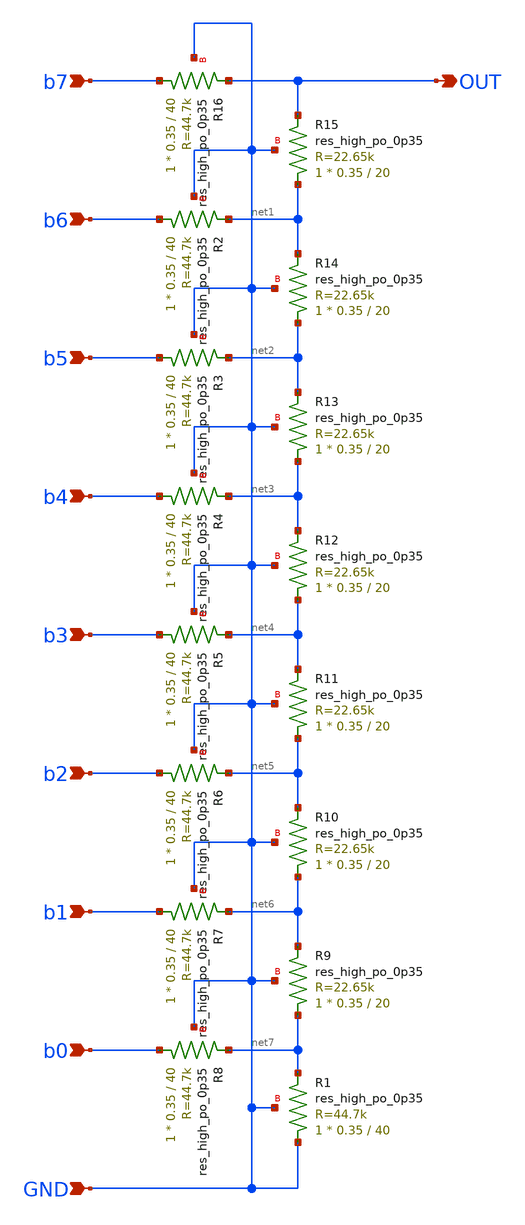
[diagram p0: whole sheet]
** sch_path: xschem/r2rdac.sch
**.subckt r2rdac b7 b6 b5 b4 b3 b2 b1 b0 GND OUT
*.ipin b7
*.ipin b6
*.ipin b5
*.ipin b4
*.ipin b3
*.ipin b2
*.ipin b1
*.ipin b0
*.ipin GND
*.opin OUT
XR16 b7 OUT GND sky130_fd_pr__res_high_po_0p35 L=40 mult=1 m=1
XR2 b6 net1 GND sky130_fd_pr__res_high_po_0p35 L=40 mult=1 m=1
XR3 b5 net2 GND sky130_fd_pr__res_high_po_0p35 L=40 mult=1 m=1
XR4 b4 net3 GND sky130_fd_pr__res_high_po_0p35 L=40 mult=1 m=1
XR5 b3 net4 GND sky130_fd_pr__res_high_po_0p35 L=40 mult=1 m=1
XR6 b2 net5 GND sky130_fd_pr__res_high_po_0p35 L=40 mult=1 m=1
XR7 b1 net6 GND sky130_fd_pr__res_high_po_0p35 L=40 mult=1 m=1
XR8 b0 net7 GND sky130_fd_pr__res_high_po_0p35 L=40 mult=1 m=1
XR1 GND net7 GND sky130_fd_pr__res_high_po_0p35 L=40 mult=1 m=1
XR9 net7 net6 GND sky130_fd_pr__res_high_po_0p35 L=20 mult=1 m=1
XR10 net6 net5 GND sky130_fd_pr__res_high_po_0p35 L=20 mult=1 m=1
XR11 net5 net4 GND sky130_fd_pr__res_high_po_0p35 L=20 mult=1 m=1
XR12 net4 net3 GND sky130_fd_pr__res_high_po_0p35 L=20 mult=1 m=1
XR13 net3 net2 GND sky130_fd_pr__res_high_po_0p35 L=20 mult=1 m=1
XR14 net2 net1 GND sky130_fd_pr__res_high_po_0p35 L=20 mult=1 m=1
XR15 net1 OUT GND sky130_fd_pr__res_high_po_0p35 L=20 mult=1 m=1
**.ends
.end
